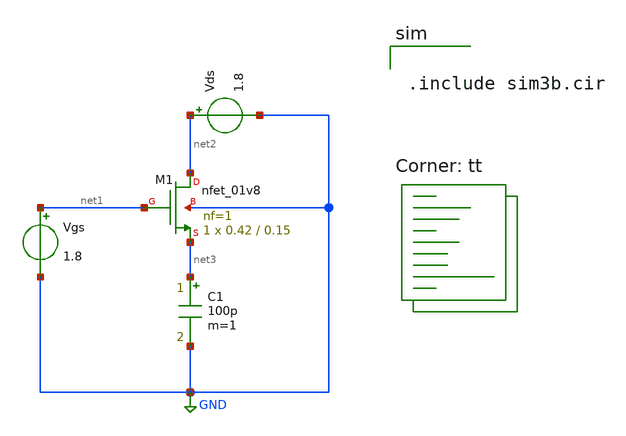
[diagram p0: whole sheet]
** sch_path: assignments/assignment1/assign3a.sch
**.subckt assign3a
XM1 net2 net1 net3 GND sky130_fd_pr__nfet_01v8 L=0.15 W=0.42 nf=1 ad='int((nf+1)/2) * W/nf * 0.29' as='int((nf+2)/2) * W/nf * 0.29'
+ pd='2*int((nf+1)/2) * (W/nf + 0.29)' ps='2*int((nf+2)/2) * (W/nf + 0.29)' nrd='0.29 / W' nrs='0.29 / W'
+ sa=0 sb=0 sd=0 mult=1 m=1
Vgs net1 GND 1.8
Vds net2 GND 1.8
C1 net3 GND 100p m=1
**** begin user architecture code


.include sim3b.cir


.lib $::SKYWATER_MODELS/sky130.lib.spice tt
**** end user architecture code
**.ends
.GLOBAL GND
.end
